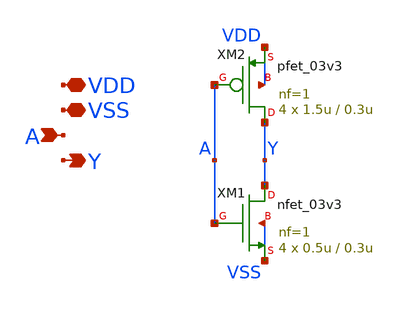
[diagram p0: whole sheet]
** sch_path: designs/libs/core_analog/switch-matrix/inv_4.sch
**.subckt inv_4 VDD VSS A Y
*.iopin VDD
*.iopin VSS
*.ipin A
*.opin Y
XM1 Y A VSS VSS nfet_03v3 L=0.3u W=0.5u nf=1 ad='int((nf+1)/2) * W/nf * 0.18u' as='int((nf+2)/2) * W/nf * 0.18u'
+ pd='2*int((nf+1)/2) * (W/nf + 0.18u)' ps='2*int((nf+2)/2) * (W/nf + 0.18u)' nrd='0.18u / W' nrs='0.18u / W'
+ sa=0 sb=0 sd=0 m=4
XM2 Y A VDD VDD pfet_03v3 L=0.3u W=1.5u nf=1 ad='int((nf+1)/2) * W/nf * 0.18u' as='int((nf+2)/2) * W/nf * 0.18u'
+ pd='2*int((nf+1)/2) * (W/nf + 0.18u)' ps='2*int((nf+2)/2) * (W/nf + 0.18u)' nrd='0.18u / W' nrs='0.18u / W'
+ sa=0 sb=0 sd=0 m=4
**.ends
.end
